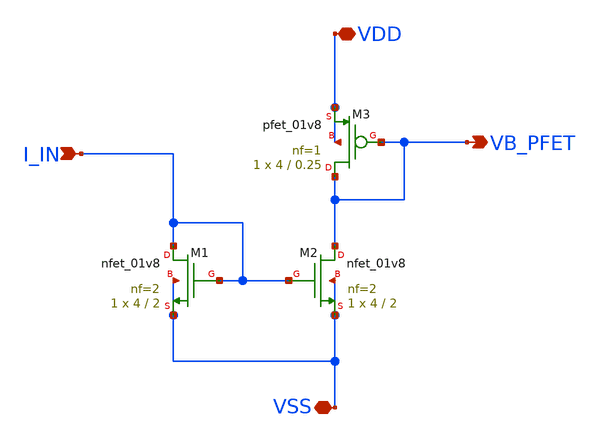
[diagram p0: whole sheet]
** sch_path: xschem/vco_bias.sch
**.subckt vco_bias VDD VSS I_IN VB_PFET
*.iopin VDD
*.iopin VSS
*.ipin I_IN
*.opin VB_PFET
XM1 I_IN I_IN VSS VSS sky130_fd_pr__nfet_01v8 L=2 W=4 nf=2 ad='int((nf+1)/2) * W/nf * 0.29' as='int((nf+2)/2) * W/nf * 0.29'
+ pd='2*int((nf+1)/2) * (W/nf + 0.29)' ps='2*int((nf+2)/2) * (W/nf + 0.29)' nrd='0.29 / W' nrs='0.29 / W'
+ sa=0 sb=0 sd=0 mult=1 m=1
XM2 VB_PFET I_IN VSS VSS sky130_fd_pr__nfet_01v8 L=2 W=4 nf=2 ad='int((nf+1)/2) * W/nf * 0.29' as='int((nf+2)/2) * W/nf * 0.29'
+ pd='2*int((nf+1)/2) * (W/nf + 0.29)' ps='2*int((nf+2)/2) * (W/nf + 0.29)' nrd='0.29 / W' nrs='0.29 / W'
+ sa=0 sb=0 sd=0 mult=1 m=1
XM3 VB_PFET VB_PFET VDD VDD sky130_fd_pr__pfet_01v8 L=0.25 W=4 nf=1 ad='int((nf+1)/2) * W/nf * 0.29'
+ as='int((nf+2)/2) * W/nf * 0.29' pd='2*int((nf+1)/2) * (W/nf + 0.29)' ps='2*int((nf+2)/2) * (W/nf + 0.29)'
+ nrd='0.29 / W' nrs='0.29 / W' sa=0 sb=0 sd=0 mult=1 m=1
**.ends
.end
